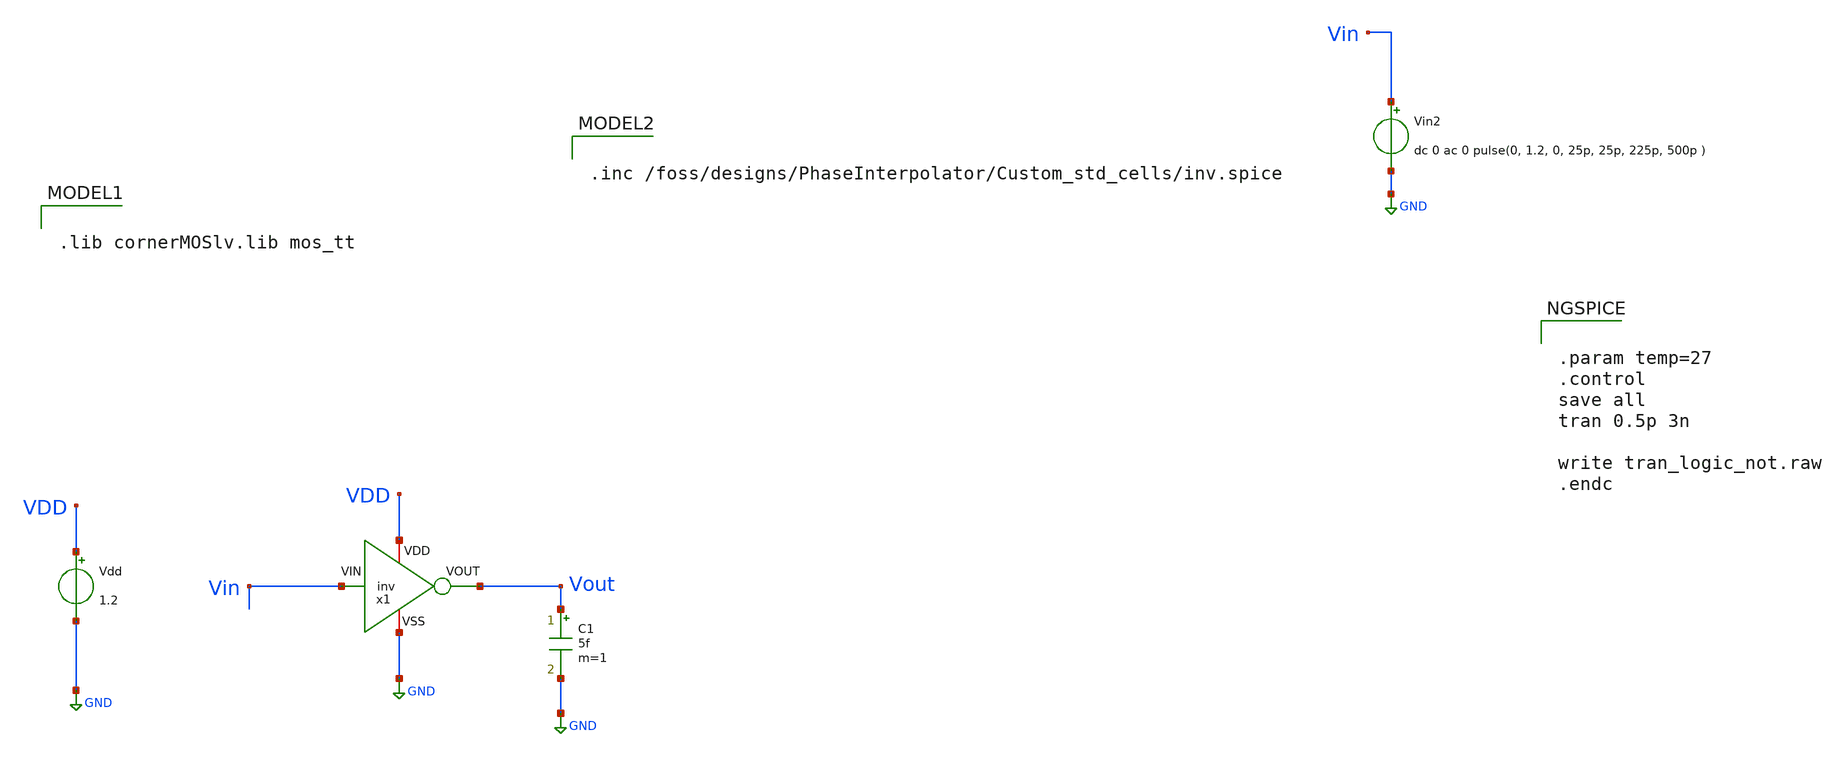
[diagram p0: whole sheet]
** sch_path: tb_inv.sch
**.subckt tb_inv
x1 VDD Vout Vin GND inv
Vdd VDD GND 1.2
C1 Vout GND 5f m=1
Vin2 Vin GND dc 0 ac 0 pulse(0, 1.2, 0, 25p, 25p, 225p, 500p )
**** begin user architecture code

.lib cornerMOSlv.lib mos_tt


.inc /foss/designs/PhaseInterpolator/Custom_std_cells/inv.spice



.param temp=27
.control
save all
tran 0.5p 3n

write tran_logic_not.raw
.endc


**** end user architecture code
**.ends
.GLOBAL GND
.end
